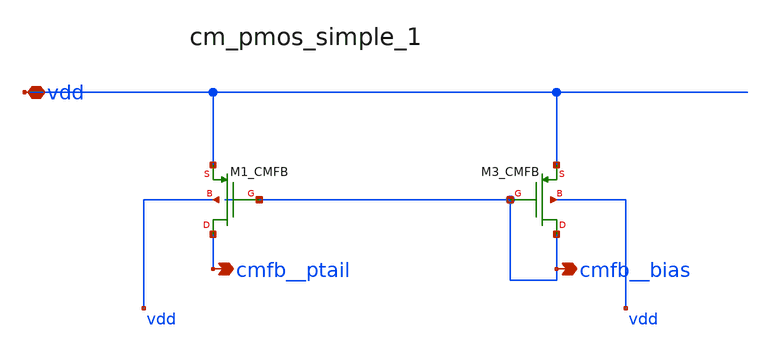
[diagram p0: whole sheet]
** sch_path: analog-db/raw/ia_006_fan_chopper_cmfb/hier/blocks/cm_pmos_simple_1.sch
**.subckt cm_pmos_simple_1 vdd cmfb__bias cmfb__ptail
*.iopin vdd
*.opin cmfb__bias
*.opin cmfb__ptail
XM1_CMFB cmfb__ptail cmfb__bias vdd vdd sg13_lv_pmos w=x_dut_xm1_cmfb_w l=x_dut_xm1_cmfb_l ng=1
+ m=x_dut_xm1_cmfb_m
XM3_CMFB cmfb__bias cmfb__bias vdd vdd sg13_lv_pmos w=x_dut_xm3_cmfb_w l=x_dut_xm3_cmfb_l ng=1
+ m=x_dut_xm3_cmfb_m
**.ends
.end
